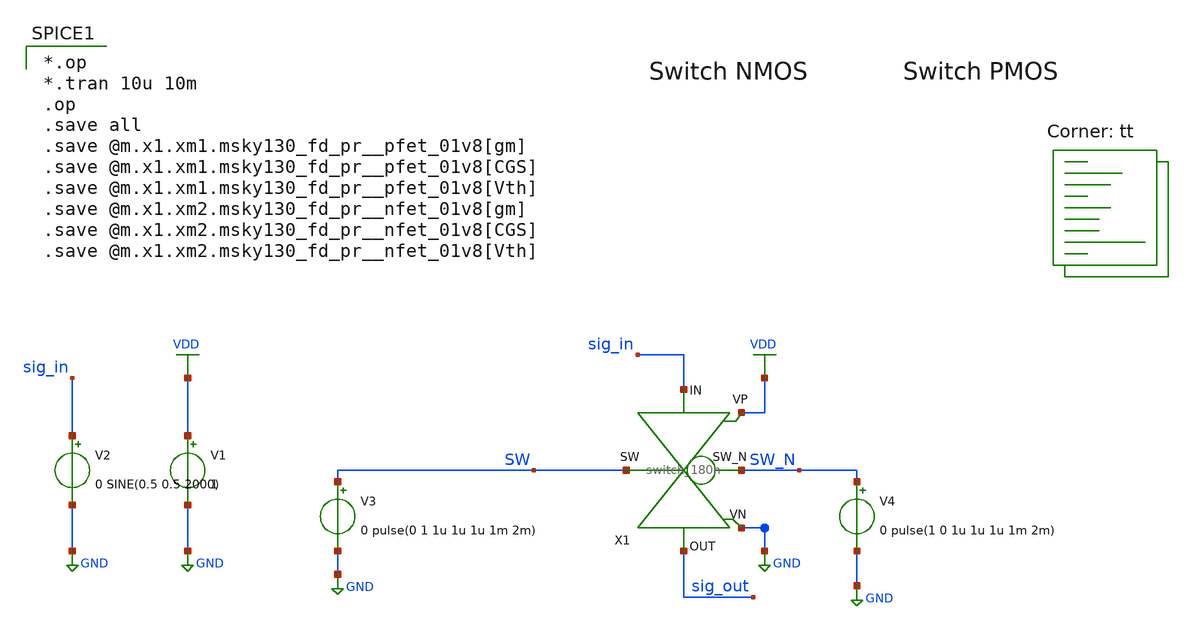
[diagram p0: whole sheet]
** sch_path: xschem/switch_180n/switch_180n_transient.sch
**.subckt switch_180n_transient
V1 VDD GND 1
V2 sig_in GND 0 SINE(0.5 0.5 2000)
V3 SW GND 0 pulse(0 1 1u 1u 1u 1m 2m)
V4 SW_N GND 0 pulse(1 0 1u 1u 1u 1m 2m)
X1 SW_N sig_in SW sig_out VDD GND switch_180n
**** begin user architecture code

*.op
*.tran 10u 10m
.op
.save all
.save @m.x1.xm1.msky130_fd_pr__pfet_01v8[gm]
.save @m.x1.xm1.msky130_fd_pr__pfet_01v8[CGS]
.save @m.x1.xm1.msky130_fd_pr__pfet_01v8[Vth]
.save @m.x1.xm2.msky130_fd_pr__nfet_01v8[gm]
.save @m.x1.xm2.msky130_fd_pr__nfet_01v8[CGS]
.save @m.x1.xm2.msky130_fd_pr__nfet_01v8[Vth]


.lib $::SKYWATER_MODELS/sky130.lib.spice tt
**** end user architecture code
**.ends
.GLOBAL GND
.GLOBAL VDD
.end
